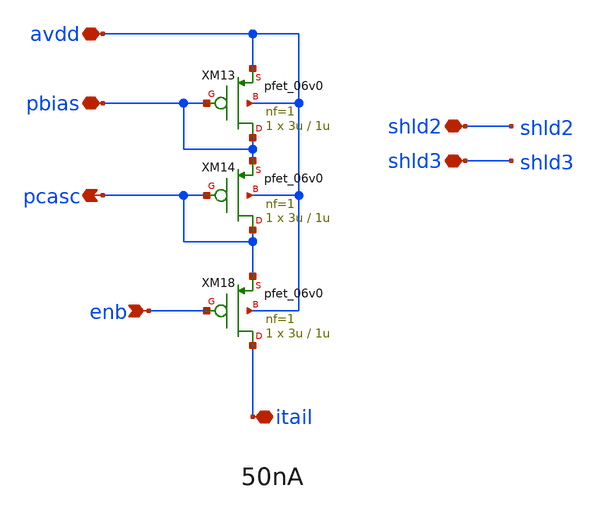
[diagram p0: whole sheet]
** sch_path: xschem/bias_pset2.sch
**.subckt bias_pset2 pbias itail enb pcasc avdd shld2 shld3
*.iopin pbias
*.iopin itail
*.ipin enb
*.opin pcasc
*.iopin avdd
*.iopin shld2
*.iopin shld3
XM13 pbias pbias avdd avdd pfet_06v0 L=1u W=3u nf=1 ad='int((nf+1)/2) * W/nf * 0.18u' as='int((nf+2)/2) * W/nf * 0.18u'
+ pd='2*int((nf+1)/2) * (W/nf + 0.18u)' ps='2*int((nf+2)/2) * (W/nf + 0.18u)' nrd='0.18u / W' nrs='0.18u / W'
+ sa=0 sb=0 sd=0 m=1
XM18 itail enb pcasc avdd pfet_06v0 L=1u W=3u nf=1 ad='int((nf+1)/2) * W/nf * 0.18u' as='int((nf+2)/2) * W/nf * 0.18u'
+ pd='2*int((nf+1)/2) * (W/nf + 0.18u)' ps='2*int((nf+2)/2) * (W/nf + 0.18u)' nrd='0.18u / W' nrs='0.18u / W'
+ sa=0 sb=0 sd=0 m=1
XM14 pcasc pcasc pbias avdd pfet_06v0 L=1u W=3u nf=1 ad='int((nf+1)/2) * W/nf * 0.18u' as='int((nf+2)/2) * W/nf * 0.18u'
+ pd='2*int((nf+1)/2) * (W/nf + 0.18u)' ps='2*int((nf+2)/2) * (W/nf + 0.18u)' nrd='0.18u / W' nrs='0.18u / W'
+ sa=0 sb=0 sd=0 m=1
**.ends
.end
